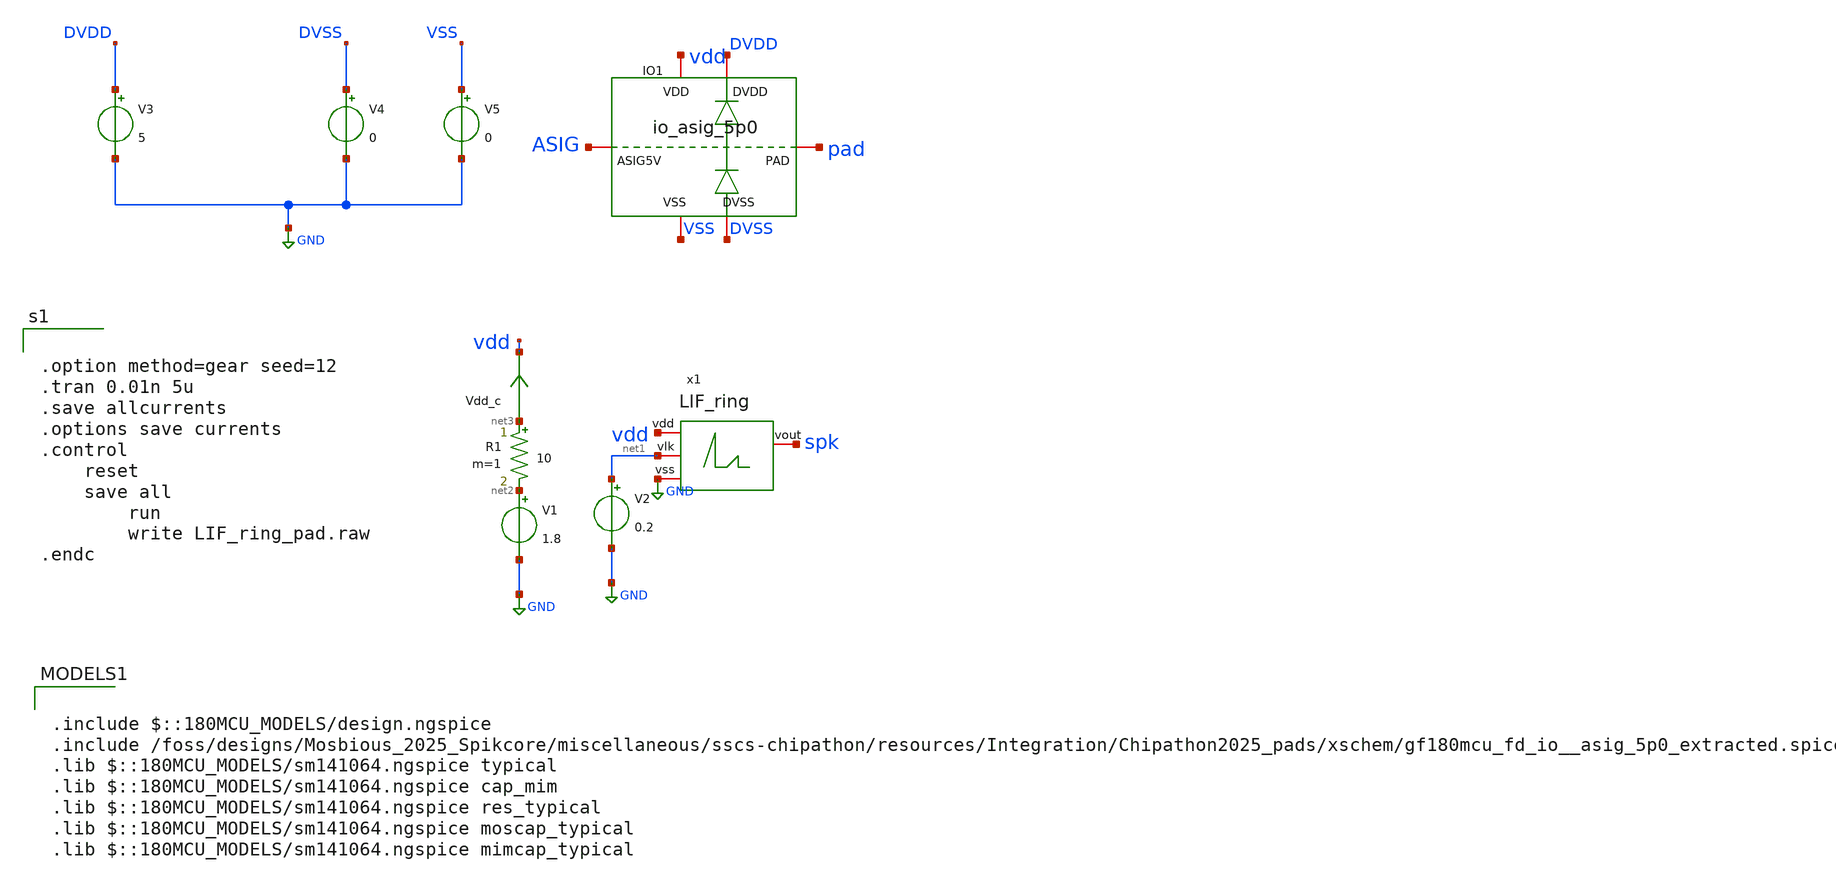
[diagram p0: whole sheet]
** sch_path: designs/libs/tb_core_analogs_pads/tb_LIF_ring/LIF_ring.sch
**.subckt LIF_ring
V1 net2 GND 1.8
Vdd_c net3 vdd 0
.save i(vdd_c)
R1 net3 net2 10 m=1
V2 net1 GND 0.2
x1 vdd net1 spk GND LIF_ring
V3 DVDD GND 5
V4 DVSS GND 0
V5 VSS GND 0
XIO1 DVSS DVDD VSS vdd pad ASIG gf180mcu_fd_io__asig_5p0_extracted
**** begin user architecture code


.option method=gear seed=12
.tran 0.01n 5u
.save allcurrents
.options save currents
.control
	reset
	save all
        run
        write LIF_ring_pad.raw
.endc



.include $::180MCU_MODELS/design.ngspice
.include /foss/designs/Mosbious_2025_Spikcore/miscellaneous/sscs-chipathon/resources/Integration/Chipathon2025_pads/xschem/gf180mcu_fd_io__asig_5p0_extracted.spice
.lib $::180MCU_MODELS/sm141064.ngspice typical
.lib $::180MCU_MODELS/sm141064.ngspice cap_mim
.lib $::180MCU_MODELS/sm141064.ngspice res_typical
.lib $::180MCU_MODELS/sm141064.ngspice moscap_typical
.lib $::180MCU_MODELS/sm141064.ngspice mimcap_typical

**** end user architecture code
**.ends
.GLOBAL GND
.end
